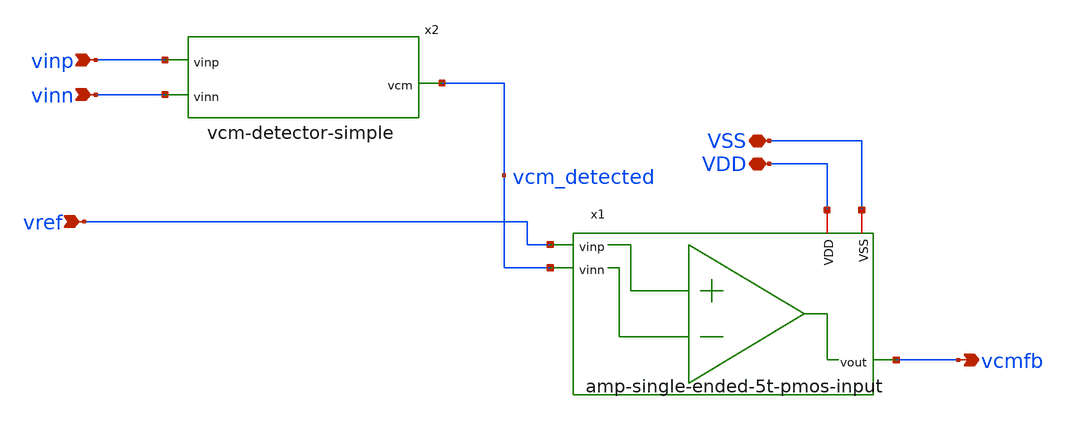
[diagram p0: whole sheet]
** sch_path: analog-db/drawings/shared/cmfb-output-amp-5t-pmos-input-inv.sch
* Copyright 2026 MacAnalog Research Group
**.subckt cmfb-output-amp-5t-pmos-input-inv VSS VDD vinp vinn vcmfb vref
*.iopin VSS
*.iopin VDD
*.ipin vinp
*.ipin vinn
*.opin vcmfb
*.ipin vref
x2 vcm_detected vinp vinn vcm-detector-simple
x1 vcmfb vref vcm_detected VSS VDD amp-single-ended-5t-pmos-input
**.ends
.end
